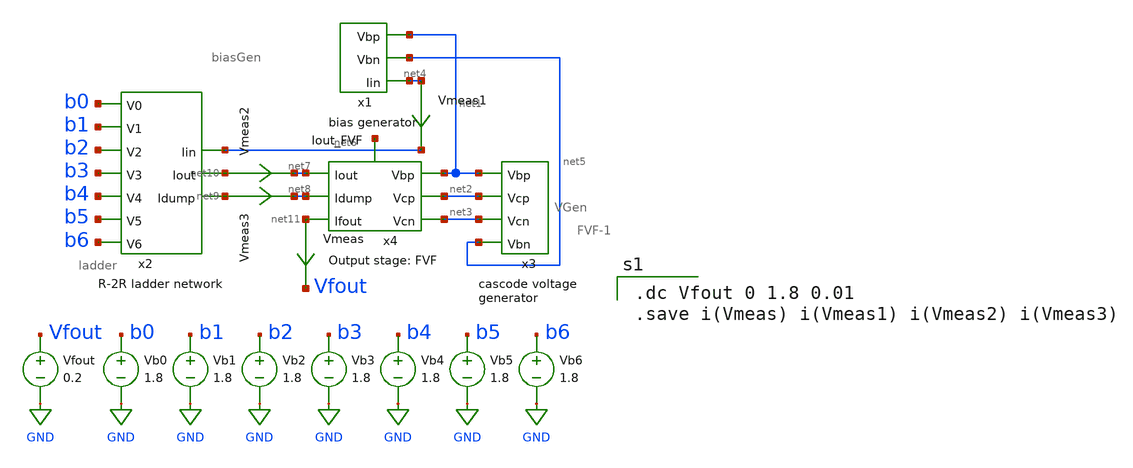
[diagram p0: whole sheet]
** sch_path: xschem/MP4-simulation-2-lauren.sch
**.subckt MP4-simulation-2-lauren
Vb0 b0 GND 1.8
x1 net1 net4 net5 biasGen
x2 net6 net9 net10 b0 b1 b2 b3 b4 b5 b6 ladder
x3 net1 net3 net2 net5 VGen
x4 net1 net2 net7 net3 net11 net8 net12 FVF-1
Vb1 b1 GND 1.8
Vb2 b2 GND 1.8
Vb3 b3 GND 1.8
Vb4 b4 GND 1.8
Vb5 b5 GND 1.8
Vb6 b6 GND 1.8
Vfout Vfout GND 0.2
Vmeas net11 Vfout 0
.save i(vmeas)
Vmeas1 net4 net6 0
.save i(vmeas1)
Vmeas2 net10 net7 0
.save i(vmeas2)
Vmeas3 net9 net8 0
.save i(vmeas3)
**** begin user architecture code

.option wnflag=1
.lib ~/skywater/skywater-pdk/libraries/sky130_fd_pr_ngspice/latest/models/sky130.lib.spice tt


.dc Vfout 0 1.8 0.01
.save i(Vmeas) i(Vmeas1) i(Vmeas2) i(Vmeas3)

**** end user architecture code
**.ends

* expanding   symbol:  /home/madvlsi/DAC-VLSI/xschem/biasGen.sym # of pins=3
** sym_path: xschem/biasGen.sym
** sch_path: xschem/biasGen.sch
.subckt biasGen Vbp Iin Vbn
*.opin Iin
*.opin Vbp
*.opin Vbn
XM1 Vbn Vbn GND GND sky130_fd_pr__nfet_01v8 L=0.15 W=1 nf=1 ad='int((nf+1)/2) * W/nf * 0.29' as='int((nf+2)/2) * W/nf * 0.29'
+ pd='2*int((nf+1)/2) * (W/nf + 0.29)' ps='2*int((nf+2)/2) * (W/nf + 0.29)' nrd='0.29 / W' nrs='0.29 / W'
+ sa=0 sb=0 sd=0 mult=1 m=1
XM2 GND Vbn Vbp GND sky130_fd_pr__nfet_01v8 L=0.15 W=1 nf=1 ad='int((nf+1)/2) * W/nf * 0.29' as='int((nf+2)/2) * W/nf * 0.29'
+ pd='2*int((nf+1)/2) * (W/nf + 0.29)' ps='2*int((nf+2)/2) * (W/nf + 0.29)' nrd='0.29 / W' nrs='0.29 / W'
+ sa=0 sb=0 sd=0 mult=1 m=1
XM3 net1 net2 GND GND sky130_fd_pr__nfet_01v8 L=0.15 W=1 nf=1 ad='int((nf+1)/2) * W/nf * 0.29' as='int((nf+2)/2) * W/nf * 0.29'
+ pd='2*int((nf+1)/2) * (W/nf + 0.29)' ps='2*int((nf+2)/2) * (W/nf + 0.29)' nrd='0.29 / W' nrs='0.29 / W'
+ sa=0 sb=0 sd=0 mult=1 m=1
XM4 net3 net2 net2 GND sky130_fd_pr__nfet_01v8 L=0.15 W=8 nf=1 ad='int((nf+1)/2) * W/nf * 0.29' as='int((nf+2)/2) * W/nf * 0.29'
+ pd='2*int((nf+1)/2) * (W/nf + 0.29)' ps='2*int((nf+2)/2) * (W/nf + 0.29)' nrd='0.29 / W' nrs='0.29 / W'
+ sa=0 sb=0 sd=0 mult=1 m=1
XM5 Vbp net1 VDD VDD sky130_fd_pr__pfet_01v8 L=0.15 W=1 nf=1 ad='int((nf+1)/2) * W/nf * 0.29' as='int((nf+2)/2) * W/nf * 0.29'
+ pd='2*int((nf+1)/2) * (W/nf + 0.29)' ps='2*int((nf+2)/2) * (W/nf + 0.29)' nrd='0.29 / W' nrs='0.29 / W'
+ sa=0 sb=0 sd=0 mult=1 m=1
XM6 VDD net1 net1 VDD sky130_fd_pr__pfet_01v8 L=0.15 W=1 nf=1 ad='int((nf+1)/2) * W/nf * 0.29' as='int((nf+2)/2) * W/nf * 0.29'
+ pd='2*int((nf+1)/2) * (W/nf + 0.29)' ps='2*int((nf+2)/2) * (W/nf + 0.29)' nrd='0.29 / W' nrs='0.29 / W'
+ sa=0 sb=0 sd=0 mult=1 m=1
XM7 VDD Vbp net2 VDD sky130_fd_pr__pfet_01v8 L=0.15 W=1 nf=1 ad='int((nf+1)/2) * W/nf * 0.29' as='int((nf+2)/2) * W/nf * 0.29'
+ pd='2*int((nf+1)/2) * (W/nf + 0.29)' ps='2*int((nf+2)/2) * (W/nf + 0.29)' nrd='0.29 / W' nrs='0.29 / W'
+ sa=0 sb=0 sd=0 mult=1 m=1
XM8 Vbn Vbp VDD VDD sky130_fd_pr__pfet_01v8 L=0.15 W=1 nf=1 ad='int((nf+1)/2) * W/nf * 0.29' as='int((nf+2)/2) * W/nf * 0.29'
+ pd='2*int((nf+1)/2) * (W/nf + 0.29)' ps='2*int((nf+2)/2) * (W/nf + 0.29)' nrd='0.29 / W' nrs='0.29 / W'
+ sa=0 sb=0 sd=0 mult=1 m=1
R1 net3 GND 100k m=1
XM9 Iin Vbp VDD VDD sky130_fd_pr__pfet_01v8 L=0.15 W=1 nf=1 ad='int((nf+1)/2) * W/nf * 0.29' as='int((nf+2)/2) * W/nf * 0.29'
+ pd='2*int((nf+1)/2) * (W/nf + 0.29)' ps='2*int((nf+2)/2) * (W/nf + 0.29)' nrd='0.29 / W' nrs='0.29 / W'
+ sa=0 sb=0 sd=0 mult=1 m=1
.ends


* expanding   symbol:  /home/madvlsi/DAC-VLSI/xschem/ladder.sym # of pins=10
** sym_path: xschem/ladder.sym
** sch_path: xschem/ladder.sch
.subckt ladder Iin Idump Iout V0 V1 V2 V3 V4 V5 V6
*.ipin Iin
*.ipin V0
*.ipin V1
*.ipin V2
*.ipin V3
*.ipin V4
*.ipin V5
*.ipin V6
*.opin Idump
*.opin Iout
XM1 Iin VDD net1 GND sky130_fd_pr__nfet_01v8 L=0.15 W=1 nf=1 ad='int((nf+1)/2) * W/nf * 0.29' as='int((nf+2)/2) * W/nf * 0.29'
+ pd='2*int((nf+1)/2) * (W/nf + 0.29)' ps='2*int((nf+2)/2) * (W/nf + 0.29)' nrd='0.29 / W' nrs='0.29 / W'
+ sa=0 sb=0 sd=0 mult=1 m=1
XM3 Iin VDD net3 GND sky130_fd_pr__nfet_01v8 L=0.15 W=1 nf=1 ad='int((nf+1)/2) * W/nf * 0.29' as='int((nf+2)/2) * W/nf * 0.29'
+ pd='2*int((nf+1)/2) * (W/nf + 0.29)' ps='2*int((nf+2)/2) * (W/nf + 0.29)' nrd='0.29 / W' nrs='0.29 / W'
+ sa=0 sb=0 sd=0 mult=1 m=1
XM5 net3 VDD net4 GND sky130_fd_pr__nfet_01v8 L=0.15 W=1 nf=1 ad='int((nf+1)/2) * W/nf * 0.29' as='int((nf+2)/2) * W/nf * 0.29'
+ pd='2*int((nf+1)/2) * (W/nf + 0.29)' ps='2*int((nf+2)/2) * (W/nf + 0.29)' nrd='0.29 / W' nrs='0.29 / W'
+ sa=0 sb=0 sd=0 mult=1 m=1
XM7 net3 VDD net6 GND sky130_fd_pr__nfet_01v8 L=0.15 W=1 nf=1 ad='int((nf+1)/2) * W/nf * 0.29' as='int((nf+2)/2) * W/nf * 0.29'
+ pd='2*int((nf+1)/2) * (W/nf + 0.29)' ps='2*int((nf+2)/2) * (W/nf + 0.29)' nrd='0.29 / W' nrs='0.29 / W'
+ sa=0 sb=0 sd=0 mult=1 m=1
XM6 net4 V1 net2 GND sky130_fd_pr__nfet_01v8 L=0.15 W=1 nf=1 ad='int((nf+1)/2) * W/nf * 0.29' as='int((nf+2)/2) * W/nf * 0.29'
+ pd='2*int((nf+1)/2) * (W/nf + 0.29)' ps='2*int((nf+2)/2) * (W/nf + 0.29)' nrd='0.29 / W' nrs='0.29 / W'
+ sa=0 sb=0 sd=0 mult=1 m=1
XM8 net4 net18 net5 GND sky130_fd_pr__nfet_01v8 L=0.15 W=1 nf=1 ad='int((nf+1)/2) * W/nf * 0.29' as='int((nf+2)/2) * W/nf * 0.29'
+ pd='2*int((nf+1)/2) * (W/nf + 0.29)' ps='2*int((nf+2)/2) * (W/nf + 0.29)' nrd='0.29 / W' nrs='0.29 / W'
+ sa=0 sb=0 sd=0 mult=1 m=1
XM2 net1 V0 net2 GND sky130_fd_pr__nfet_01v8 L=0.15 W=1 nf=1 ad='int((nf+1)/2) * W/nf * 0.29' as='int((nf+2)/2) * W/nf * 0.29'
+ pd='2*int((nf+1)/2) * (W/nf + 0.29)' ps='2*int((nf+2)/2) * (W/nf + 0.29)' nrd='0.29 / W' nrs='0.29 / W'
+ sa=0 sb=0 sd=0 mult=1 m=1
XM4 net1 net17 net5 GND sky130_fd_pr__nfet_01v8 L=0.15 W=1 nf=1 ad='int((nf+1)/2) * W/nf * 0.29' as='int((nf+2)/2) * W/nf * 0.29'
+ pd='2*int((nf+1)/2) * (W/nf + 0.29)' ps='2*int((nf+2)/2) * (W/nf + 0.29)' nrd='0.29 / W' nrs='0.29 / W'
+ sa=0 sb=0 sd=0 mult=1 m=1
XM9 net6 VDD net7 GND sky130_fd_pr__nfet_01v8 L=0.15 W=1 nf=1 ad='int((nf+1)/2) * W/nf * 0.29' as='int((nf+2)/2) * W/nf * 0.29'
+ pd='2*int((nf+1)/2) * (W/nf + 0.29)' ps='2*int((nf+2)/2) * (W/nf + 0.29)' nrd='0.29 / W' nrs='0.29 / W'
+ sa=0 sb=0 sd=0 mult=1 m=1
XM11 net6 VDD net8 GND sky130_fd_pr__nfet_01v8 L=0.15 W=1 nf=1 ad='int((nf+1)/2) * W/nf * 0.29' as='int((nf+2)/2) * W/nf * 0.29'
+ pd='2*int((nf+1)/2) * (W/nf + 0.29)' ps='2*int((nf+2)/2) * (W/nf + 0.29)' nrd='0.29 / W' nrs='0.29 / W'
+ sa=0 sb=0 sd=0 mult=1 m=1
XM10 net7 V2 net2 GND sky130_fd_pr__nfet_01v8 L=0.15 W=1 nf=1 ad='int((nf+1)/2) * W/nf * 0.29' as='int((nf+2)/2) * W/nf * 0.29'
+ pd='2*int((nf+1)/2) * (W/nf + 0.29)' ps='2*int((nf+2)/2) * (W/nf + 0.29)' nrd='0.29 / W' nrs='0.29 / W'
+ sa=0 sb=0 sd=0 mult=1 m=1
XM12 net7 net19 net5 GND sky130_fd_pr__nfet_01v8 L=0.15 W=1 nf=1 ad='int((nf+1)/2) * W/nf * 0.29' as='int((nf+2)/2) * W/nf * 0.29'
+ pd='2*int((nf+1)/2) * (W/nf + 0.29)' ps='2*int((nf+2)/2) * (W/nf + 0.29)' nrd='0.29 / W' nrs='0.29 / W'
+ sa=0 sb=0 sd=0 mult=1 m=1
XM13 net8 VDD net9 GND sky130_fd_pr__nfet_01v8 L=0.15 W=1 nf=1 ad='int((nf+1)/2) * W/nf * 0.29' as='int((nf+2)/2) * W/nf * 0.29'
+ pd='2*int((nf+1)/2) * (W/nf + 0.29)' ps='2*int((nf+2)/2) * (W/nf + 0.29)' nrd='0.29 / W' nrs='0.29 / W'
+ sa=0 sb=0 sd=0 mult=1 m=1
XM15 net8 VDD net10 GND sky130_fd_pr__nfet_01v8 L=0.15 W=1 nf=1 ad='int((nf+1)/2) * W/nf * 0.29' as='int((nf+2)/2) * W/nf * 0.29'
+ pd='2*int((nf+1)/2) * (W/nf + 0.29)' ps='2*int((nf+2)/2) * (W/nf + 0.29)' nrd='0.29 / W' nrs='0.29 / W'
+ sa=0 sb=0 sd=0 mult=1 m=1
XM14 net9 V3 net2 GND sky130_fd_pr__nfet_01v8 L=0.15 W=1 nf=1 ad='int((nf+1)/2) * W/nf * 0.29' as='int((nf+2)/2) * W/nf * 0.29'
+ pd='2*int((nf+1)/2) * (W/nf + 0.29)' ps='2*int((nf+2)/2) * (W/nf + 0.29)' nrd='0.29 / W' nrs='0.29 / W'
+ sa=0 sb=0 sd=0 mult=1 m=1
XM16 net9 net20 net5 GND sky130_fd_pr__nfet_01v8 L=0.15 W=1 nf=1 ad='int((nf+1)/2) * W/nf * 0.29' as='int((nf+2)/2) * W/nf * 0.29'
+ pd='2*int((nf+1)/2) * (W/nf + 0.29)' ps='2*int((nf+2)/2) * (W/nf + 0.29)' nrd='0.29 / W' nrs='0.29 / W'
+ sa=0 sb=0 sd=0 mult=1 m=1
XM17 net10 VDD net11 GND sky130_fd_pr__nfet_01v8 L=0.15 W=1 nf=1 ad='int((nf+1)/2) * W/nf * 0.29' as='int((nf+2)/2) * W/nf * 0.29'
+ pd='2*int((nf+1)/2) * (W/nf + 0.29)' ps='2*int((nf+2)/2) * (W/nf + 0.29)' nrd='0.29 / W' nrs='0.29 / W'
+ sa=0 sb=0 sd=0 mult=1 m=1
XM19 net10 VDD net12 GND sky130_fd_pr__nfet_01v8 L=0.15 W=1 nf=1 ad='int((nf+1)/2) * W/nf * 0.29' as='int((nf+2)/2) * W/nf * 0.29'
+ pd='2*int((nf+1)/2) * (W/nf + 0.29)' ps='2*int((nf+2)/2) * (W/nf + 0.29)' nrd='0.29 / W' nrs='0.29 / W'
+ sa=0 sb=0 sd=0 mult=1 m=1
XM18 net11 V4 net2 GND sky130_fd_pr__nfet_01v8 L=0.15 W=1 nf=1 ad='int((nf+1)/2) * W/nf * 0.29' as='int((nf+2)/2) * W/nf * 0.29'
+ pd='2*int((nf+1)/2) * (W/nf + 0.29)' ps='2*int((nf+2)/2) * (W/nf + 0.29)' nrd='0.29 / W' nrs='0.29 / W'
+ sa=0 sb=0 sd=0 mult=1 m=1
XM20 net11 net21 net5 GND sky130_fd_pr__nfet_01v8 L=0.15 W=1 nf=1 ad='int((nf+1)/2) * W/nf * 0.29' as='int((nf+2)/2) * W/nf * 0.29'
+ pd='2*int((nf+1)/2) * (W/nf + 0.29)' ps='2*int((nf+2)/2) * (W/nf + 0.29)' nrd='0.29 / W' nrs='0.29 / W'
+ sa=0 sb=0 sd=0 mult=1 m=1
XM21 net12 VDD net13 GND sky130_fd_pr__nfet_01v8 L=0.15 W=1 nf=1 ad='int((nf+1)/2) * W/nf * 0.29' as='int((nf+2)/2) * W/nf * 0.29'
+ pd='2*int((nf+1)/2) * (W/nf + 0.29)' ps='2*int((nf+2)/2) * (W/nf + 0.29)' nrd='0.29 / W' nrs='0.29 / W'
+ sa=0 sb=0 sd=0 mult=1 m=1
XM23 net12 VDD net14 GND sky130_fd_pr__nfet_01v8 L=0.15 W=1 nf=1 ad='int((nf+1)/2) * W/nf * 0.29' as='int((nf+2)/2) * W/nf * 0.29'
+ pd='2*int((nf+1)/2) * (W/nf + 0.29)' ps='2*int((nf+2)/2) * (W/nf + 0.29)' nrd='0.29 / W' nrs='0.29 / W'
+ sa=0 sb=0 sd=0 mult=1 m=1
XM22 net13 V5 net2 GND sky130_fd_pr__nfet_01v8 L=0.15 W=1 nf=1 ad='int((nf+1)/2) * W/nf * 0.29' as='int((nf+2)/2) * W/nf * 0.29'
+ pd='2*int((nf+1)/2) * (W/nf + 0.29)' ps='2*int((nf+2)/2) * (W/nf + 0.29)' nrd='0.29 / W' nrs='0.29 / W'
+ sa=0 sb=0 sd=0 mult=1 m=1
XM24 net13 net22 net5 GND sky130_fd_pr__nfet_01v8 L=0.15 W=1 nf=1 ad='int((nf+1)/2) * W/nf * 0.29' as='int((nf+2)/2) * W/nf * 0.29'
+ pd='2*int((nf+1)/2) * (W/nf + 0.29)' ps='2*int((nf+2)/2) * (W/nf + 0.29)' nrd='0.29 / W' nrs='0.29 / W'
+ sa=0 sb=0 sd=0 mult=1 m=1
XM25 net14 VDD net15 GND sky130_fd_pr__nfet_01v8 L=0.15 W=1 nf=1 ad='int((nf+1)/2) * W/nf * 0.29' as='int((nf+2)/2) * W/nf * 0.29'
+ pd='2*int((nf+1)/2) * (W/nf + 0.29)' ps='2*int((nf+2)/2) * (W/nf + 0.29)' nrd='0.29 / W' nrs='0.29 / W'
+ sa=0 sb=0 sd=0 mult=1 m=1
XM27 net14 VDD net16 GND sky130_fd_pr__nfet_01v8 L=0.15 W=1 nf=1 ad='int((nf+1)/2) * W/nf * 0.29' as='int((nf+2)/2) * W/nf * 0.29'
+ pd='2*int((nf+1)/2) * (W/nf + 0.29)' ps='2*int((nf+2)/2) * (W/nf + 0.29)' nrd='0.29 / W' nrs='0.29 / W'
+ sa=0 sb=0 sd=0 mult=1 m=1
XM26 net15 V6 net2 GND sky130_fd_pr__nfet_01v8 L=0.15 W=1 nf=1 ad='int((nf+1)/2) * W/nf * 0.29' as='int((nf+2)/2) * W/nf * 0.29'
+ pd='2*int((nf+1)/2) * (W/nf + 0.29)' ps='2*int((nf+2)/2) * (W/nf + 0.29)' nrd='0.29 / W' nrs='0.29 / W'
+ sa=0 sb=0 sd=0 mult=1 m=1
XM28 net15 net23 net5 GND sky130_fd_pr__nfet_01v8 L=0.15 W=1 nf=1 ad='int((nf+1)/2) * W/nf * 0.29' as='int((nf+2)/2) * W/nf * 0.29'
+ pd='2*int((nf+1)/2) * (W/nf + 0.29)' ps='2*int((nf+2)/2) * (W/nf + 0.29)' nrd='0.29 / W' nrs='0.29 / W'
+ sa=0 sb=0 sd=0 mult=1 m=1
XM29 net16 VDD net5 GND sky130_fd_pr__nfet_01v8 L=0.15 W=1 nf=1 ad='int((nf+1)/2) * W/nf * 0.29' as='int((nf+2)/2) * W/nf * 0.29'
+ pd='2*int((nf+1)/2) * (W/nf + 0.29)' ps='2*int((nf+2)/2) * (W/nf + 0.29)' nrd='0.29 / W' nrs='0.29 / W'
+ sa=0 sb=0 sd=0 mult=1 m=1
XM30 GND net5 net5 GND sky130_fd_pr__nfet_01v8 L=0.15 W=1 nf=1 ad='int((nf+1)/2) * W/nf * 0.29' as='int((nf+2)/2) * W/nf * 0.29'
+ pd='2*int((nf+1)/2) * (W/nf + 0.29)' ps='2*int((nf+2)/2) * (W/nf + 0.29)' nrd='0.29 / W' nrs='0.29 / W'
+ sa=0 sb=0 sd=0 mult=1 m=1
XM31 GND net2 net2 GND sky130_fd_pr__nfet_01v8 L=0.15 W=1 nf=1 ad='int((nf+1)/2) * W/nf * 0.29' as='int((nf+2)/2) * W/nf * 0.29'
+ pd='2*int((nf+1)/2) * (W/nf + 0.29)' ps='2*int((nf+2)/2) * (W/nf + 0.29)' nrd='0.29 / W' nrs='0.29 / W'
+ sa=0 sb=0 sd=0 mult=1 m=1
XM32 Idump net5 GND GND sky130_fd_pr__nfet_01v8 L=0.15 W=1 nf=1 ad='int((nf+1)/2) * W/nf * 0.29' as='int((nf+2)/2) * W/nf * 0.29'
+ pd='2*int((nf+1)/2) * (W/nf + 0.29)' ps='2*int((nf+2)/2) * (W/nf + 0.29)' nrd='0.29 / W' nrs='0.29 / W'
+ sa=0 sb=0 sd=0 mult=1 m=1
XM33 Iout net2 GND GND sky130_fd_pr__nfet_01v8 L=0.15 W=1 nf=1 ad='int((nf+1)/2) * W/nf * 0.29' as='int((nf+2)/2) * W/nf * 0.29'
+ pd='2*int((nf+1)/2) * (W/nf + 0.29)' ps='2*int((nf+2)/2) * (W/nf + 0.29)' nrd='0.29 / W' nrs='0.29 / W'
+ sa=0 sb=0 sd=0 mult=1 m=1
x1 net17 V0 inverter
x2 net18 V1 inverter
x3 net19 V2 inverter
x4 net20 V3 inverter
x5 net21 V4 inverter
x6 net22 V5 inverter
x7 net23 V6 inverter
.ends


* expanding   symbol:  /home/madvlsi/DAC-VLSI/xschem/VGen.sym # of pins=4
** sym_path: xschem/VGen.sym
** sch_path: xschem/VGen.sch
.subckt VGen Vbp Vcn Vcp Vbn
*.opin Vcp
*.ipin Vbp
*.ipin Vbn
*.opin Vcn
XM5 net4 net4 net1 GND sky130_fd_pr__nfet_01v8 L=8 W=96 nf=1 ad='int((nf+1)/2) * W/nf * 0.29' as='int((nf+2)/2) * W/nf * 0.29'
+ pd='2*int((nf+1)/2) * (W/nf + 0.29)' ps='2*int((nf+2)/2) * (W/nf + 0.29)' nrd='0.29 / W' nrs='0.29 / W'
+ sa=0 sb=0 sd=0 mult=1 m=1
XM6 net1 net4 GND GND sky130_fd_pr__nfet_01v8 L=8 W=24 nf=1 ad='int((nf+1)/2) * W/nf * 0.29' as='int((nf+2)/2) * W/nf * 0.29'
+ pd='2*int((nf+1)/2) * (W/nf + 0.29)' ps='2*int((nf+2)/2) * (W/nf + 0.29)' nrd='0.29 / W' nrs='0.29 / W'
+ sa=0 sb=0 sd=0 mult=1 m=1
XM4 net1 Vcn Vcn GND sky130_fd_pr__nfet_01v8 L=8 W=24 nf=1 ad='int((nf+1)/2) * W/nf * 0.29' as='int((nf+2)/2) * W/nf * 0.29'
+ pd='2*int((nf+1)/2) * (W/nf + 0.29)' ps='2*int((nf+2)/2) * (W/nf + 0.29)' nrd='0.29 / W' nrs='0.29 / W'
+ sa=0 sb=0 sd=0 mult=1 m=1
XM1 VDD Vbp net4 VDD sky130_fd_pr__pfet_01v8 L=32 W=24 nf=1 ad='int((nf+1)/2) * W/nf * 0.29' as='int((nf+2)/2) * W/nf * 0.29'
+ pd='2*int((nf+1)/2) * (W/nf + 0.29)' ps='2*int((nf+2)/2) * (W/nf + 0.29)' nrd='0.29 / W' nrs='0.29 / W'
+ sa=0 sb=0 sd=0 mult=1 m=1
XM2 VDD Vbp Vcn VDD sky130_fd_pr__pfet_01v8 L=8 W=24 nf=1 ad='int((nf+1)/2) * W/nf * 0.29' as='int((nf+2)/2) * W/nf * 0.29'
+ pd='2*int((nf+1)/2) * (W/nf + 0.29)' ps='2*int((nf+2)/2) * (W/nf + 0.29)' nrd='0.29 / W' nrs='0.29 / W'
+ sa=0 sb=0 sd=0 mult=1 m=1
XM9 net3 net3 net2 VDD sky130_fd_pr__pfet_01v8 L=8 W=96 nf=1 ad='int((nf+1)/2) * W/nf * 0.29' as='int((nf+2)/2) * W/nf * 0.29'
+ pd='2*int((nf+1)/2) * (W/nf + 0.29)' ps='2*int((nf+2)/2) * (W/nf + 0.29)' nrd='0.29 / W' nrs='0.29 / W'
+ sa=0 sb=0 sd=0 mult=1 m=1
XM11 GND Vbn Vcp GND sky130_fd_pr__nfet_01v8 L=8 W=24 nf=1 ad='int((nf+1)/2) * W/nf * 0.29' as='int((nf+2)/2) * W/nf * 0.29'
+ pd='2*int((nf+1)/2) * (W/nf + 0.29)' ps='2*int((nf+2)/2) * (W/nf + 0.29)' nrd='0.29 / W' nrs='0.29 / W'
+ sa=0 sb=0 sd=0 mult=1 m=1
XM8 net2 Vcp Vcp VDD sky130_fd_pr__pfet_01v8 L=8 W=24 nf=1 ad='int((nf+1)/2) * W/nf * 0.29' as='int((nf+2)/2) * W/nf * 0.29'
+ pd='2*int((nf+1)/2) * (W/nf + 0.29)' ps='2*int((nf+2)/2) * (W/nf + 0.29)' nrd='0.29 / W' nrs='0.29 / W'
+ sa=0 sb=0 sd=0 mult=1 m=1
XM12 GND Vbn net3 GND sky130_fd_pr__nfet_01v8 L=32 W=24 nf=1 ad='int((nf+1)/2) * W/nf * 0.29' as='int((nf+2)/2) * W/nf * 0.29'
+ pd='2*int((nf+1)/2) * (W/nf + 0.29)' ps='2*int((nf+2)/2) * (W/nf + 0.29)' nrd='0.29 / W' nrs='0.29 / W'
+ sa=0 sb=0 sd=0 mult=1 m=1
XM7 net2 net3 VDD VDD sky130_fd_pr__pfet_01v8 L=8 W=24 nf=1 ad='int((nf+1)/2) * W/nf * 0.29' as='int((nf+2)/2) * W/nf * 0.29'
+ pd='2*int((nf+1)/2) * (W/nf + 0.29)' ps='2*int((nf+2)/2) * (W/nf + 0.29)' nrd='0.29 / W' nrs='0.29 / W'
+ sa=0 sb=0 sd=0 mult=1 m=1
.ends


* expanding   symbol:  /home/madvlsi/DAC-VLSI/xschem/FVF-1.sym # of pins=7
** sym_path: xschem/old_files/FVF-1.sym
** sch_path: xschem/old_files/FVF-1.sch
.subckt FVF-1 Vbp Vcp Iout Vcn Ifout Idump Iout_FVF
*.ipin Vcn
*.ipin Iout
*.ipin Idump
*.ipin Vcp
*.ipin Vbp
*.opin Ifout
*.opin Iout_FVF
XM1 net1 Vcn Idump GND sky130_fd_pr__nfet_01v8 L=8 W=24 nf=1 ad='int((nf+1)/2) * W/nf * 0.29' as='int((nf+2)/2) * W/nf * 0.29'
+ pd='2*int((nf+1)/2) * (W/nf + 0.29)' ps='2*int((nf+2)/2) * (W/nf + 0.29)' nrd='0.29 / W' nrs='0.29 / W'
+ sa=0 sb=0 sd=0 mult=1 m=1
XM2 GND net1 Idump GND sky130_fd_pr__nfet_01v8 L=8 W=24 nf=1 ad='int((nf+1)/2) * W/nf * 0.29' as='int((nf+2)/2) * W/nf * 0.29'
+ pd='2*int((nf+1)/2) * (W/nf + 0.29)' ps='2*int((nf+2)/2) * (W/nf + 0.29)' nrd='0.29 / W' nrs='0.29 / W'
+ sa=0 sb=0 sd=0 mult=1 m=1
XM3 Iout_FVF Vcn Iout GND sky130_fd_pr__nfet_01v8 L=8 W=24 nf=1 ad='int((nf+1)/2) * W/nf * 0.29' as='int((nf+2)/2) * W/nf * 0.29'
+ pd='2*int((nf+1)/2) * (W/nf + 0.29)' ps='2*int((nf+2)/2) * (W/nf + 0.29)' nrd='0.29 / W' nrs='0.29 / W'
+ sa=0 sb=0 sd=0 mult=1 m=1
XM4 GND Iout_FVF Iout GND sky130_fd_pr__nfet_01v8 L=8 W=24 nf=1 ad='int((nf+1)/2) * W/nf * 0.29' as='int((nf+2)/2) * W/nf * 0.29'
+ pd='2*int((nf+1)/2) * (W/nf + 0.29)' ps='2*int((nf+2)/2) * (W/nf + 0.29)' nrd='0.29 / W' nrs='0.29 / W'
+ sa=0 sb=0 sd=0 mult=1 m=1
XM5 Ifout Vcn net2 GND sky130_fd_pr__nfet_01v8 L=8 W=24 nf=1 ad='int((nf+1)/2) * W/nf * 0.29' as='int((nf+2)/2) * W/nf * 0.29'
+ pd='2*int((nf+1)/2) * (W/nf + 0.29)' ps='2*int((nf+2)/2) * (W/nf + 0.29)' nrd='0.29 / W' nrs='0.29 / W'
+ sa=0 sb=0 sd=0 mult=1 m=1
XM6 net2 Iout_FVF GND GND sky130_fd_pr__nfet_01v8 L=8 W=24 nf=1 ad='int((nf+1)/2) * W/nf * 0.29' as='int((nf+2)/2) * W/nf * 0.29'
+ pd='2*int((nf+1)/2) * (W/nf + 0.29)' ps='2*int((nf+2)/2) * (W/nf + 0.29)' nrd='0.29 / W' nrs='0.29 / W'
+ sa=0 sb=0 sd=0 mult=1 m=1
XM7 net1 Vcp net3 VDD sky130_fd_pr__pfet_01v8 L=8 W=24 nf=1 ad='int((nf+1)/2) * W/nf * 0.29' as='int((nf+2)/2) * W/nf * 0.29'
+ pd='2*int((nf+1)/2) * (W/nf + 0.29)' ps='2*int((nf+2)/2) * (W/nf + 0.29)' nrd='0.29 / W' nrs='0.29 / W'
+ sa=0 sb=0 sd=0 mult=1 m=1
XM8 Iout_FVF Vcp net4 VDD sky130_fd_pr__pfet_01v8 L=8 W=24 nf=1 ad='int((nf+1)/2) * W/nf * 0.29' as='int((nf+2)/2) * W/nf * 0.29'
+ pd='2*int((nf+1)/2) * (W/nf + 0.29)' ps='2*int((nf+2)/2) * (W/nf + 0.29)' nrd='0.29 / W' nrs='0.29 / W'
+ sa=0 sb=0 sd=0 mult=1 m=1
XM9 Ifout Vcp net5 VDD sky130_fd_pr__pfet_01v8 L=8 W=24 nf=1 ad='int((nf+1)/2) * W/nf * 0.29' as='int((nf+2)/2) * W/nf * 0.29'
+ pd='2*int((nf+1)/2) * (W/nf + 0.29)' ps='2*int((nf+2)/2) * (W/nf + 0.29)' nrd='0.29 / W' nrs='0.29 / W'
+ sa=0 sb=0 sd=0 mult=1 m=1
XM15 net3 Vbp VDD VDD sky130_fd_pr__pfet_01v8 L=8 W=24 nf=1 ad='int((nf+1)/2) * W/nf * 0.29' as='int((nf+2)/2) * W/nf * 0.29'
+ pd='2*int((nf+1)/2) * (W/nf + 0.29)' ps='2*int((nf+2)/2) * (W/nf + 0.29)' nrd='0.29 / W' nrs='0.29 / W'
+ sa=0 sb=0 sd=0 mult=1 m=1
XM16 net4 Vbp VDD VDD sky130_fd_pr__pfet_01v8 L=8 W=24 nf=1 ad='int((nf+1)/2) * W/nf * 0.29' as='int((nf+2)/2) * W/nf * 0.29'
+ pd='2*int((nf+1)/2) * (W/nf + 0.29)' ps='2*int((nf+2)/2) * (W/nf + 0.29)' nrd='0.29 / W' nrs='0.29 / W'
+ sa=0 sb=0 sd=0 mult=1 m=1
XM17 net5 Vbp VDD VDD sky130_fd_pr__pfet_01v8 L=8 W=24 nf=1 ad='int((nf+1)/2) * W/nf * 0.29' as='int((nf+2)/2) * W/nf * 0.29'
+ pd='2*int((nf+1)/2) * (W/nf + 0.29)' ps='2*int((nf+2)/2) * (W/nf + 0.29)' nrd='0.29 / W' nrs='0.29 / W'
+ sa=0 sb=0 sd=0 mult=1 m=1
.ends


* expanding   symbol:  ./inverter.sym # of pins=2
** sym_path: xschem/inverter.sym
** sch_path: xschem/inverter.sch
.subckt inverter Y A
*.ipin A
*.opin Y
XM1 Y A VDD VDD sky130_fd_pr__pfet_01v8 L=0.15 W=1 nf=1 ad='int((nf+1)/2) * W/nf * 0.29' as='int((nf+2)/2) * W/nf * 0.29'
+ pd='2*int((nf+1)/2) * (W/nf + 0.29)' ps='2*int((nf+2)/2) * (W/nf + 0.29)' nrd='0.29 / W' nrs='0.29 / W'
+ sa=0 sb=0 sd=0 mult=1 m=1
XM2 Y A GND GND sky130_fd_pr__nfet_01v8 L=0.15 W=1 nf=1 ad='int((nf+1)/2) * W/nf * 0.29' as='int((nf+2)/2) * W/nf * 0.29'
+ pd='2*int((nf+1)/2) * (W/nf + 0.29)' ps='2*int((nf+2)/2) * (W/nf + 0.29)' nrd='0.29 / W' nrs='0.29 / W'
+ sa=0 sb=0 sd=0 mult=1 m=1
.ends

.GLOBAL GND
.GLOBAL VDD
.end
